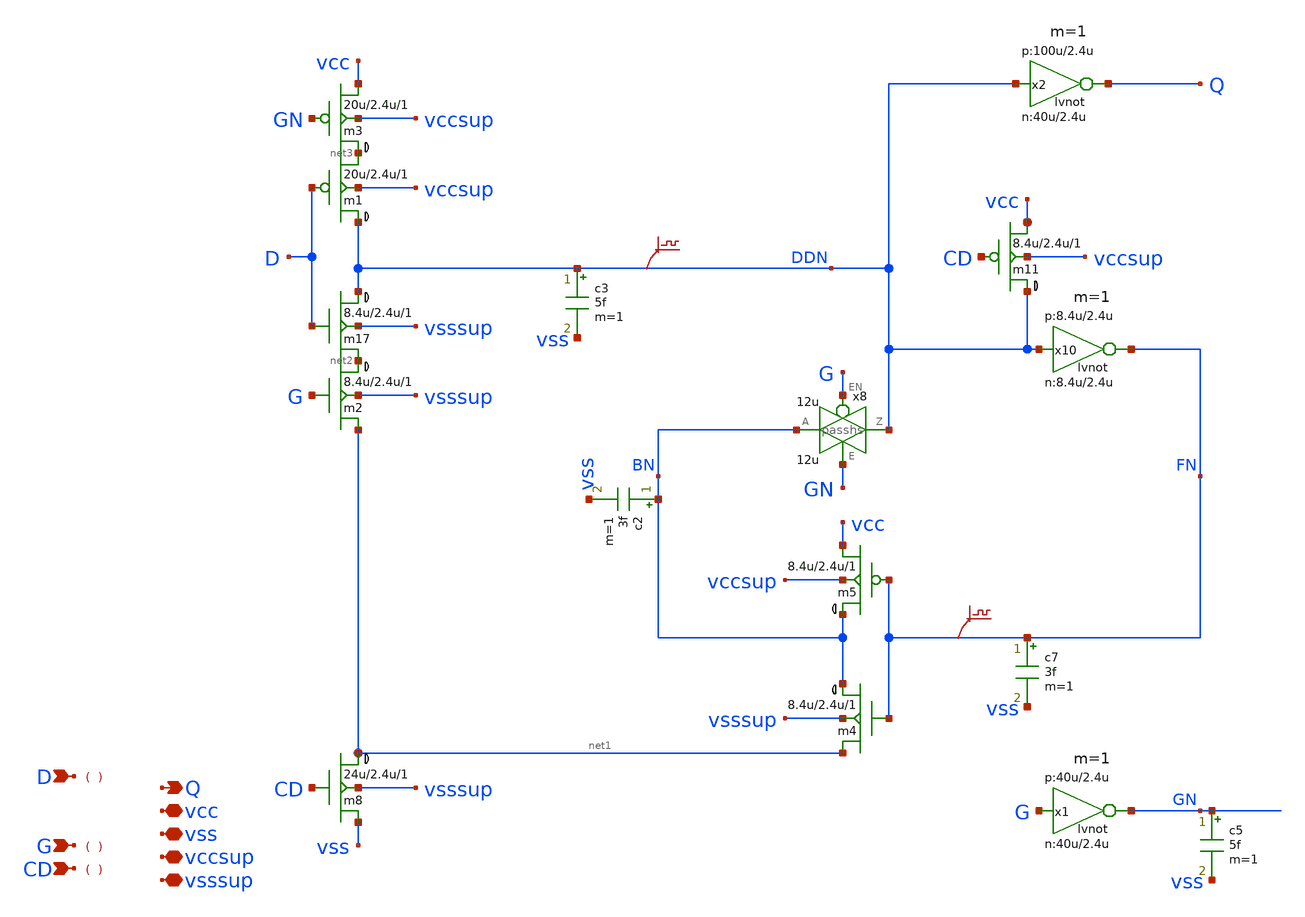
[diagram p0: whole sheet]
** sch_path: xschem-src/xschem_library/rom8k/LD2QHDX4stef.sch
* Copyright (C) 1998-2026 Stefan Frederik Schippers
* This program is free software; you can redistribute it and/or modify
* it under the terms of the GNU General Public License as published by
* the Free Software Foundation; either version 2 of the License, or
* (at your option) any later version.
* This program is distributed in the hope that it will be useful,
* but WITHOUT ANY WARRANTY; without even the implied warranty of
* MERCHANTABILITY or FITNESS FOR A PARTICULAR PURPOSE.  See the
* GNU General Public License for more details.
* You should have received a copy of the GNU General Public License
* along with this program; if not, write to the Free Software
**.subckt LD2QHDX4stef D G CD Q vcc vss vccsup vsssup
*.ipin D
*.ipin G
*.ipin CD
*.opin Q
*.iopin vcc
*.iopin vss
*.iopin vccsup
*.iopin vsssup
c2 BN vss 3f m=1
c3 DDN vss 5f m=1
c5 GN vss 5f m=1
c7 FN vss 3f m=1
x8 DDN BN G GN vccsup vsssup passhs WN=12u LN=1.2u WP=12u LP=1.2u
m17 DDN D net2 vsssup cmosn w=8.4u l=2.4u ad={8.4u *2.2u} as={8.4u *2.2u} pd={8.4u *2+4.4u} ps={8.4u *2+4.4u}
+ m=1
m1 DDN D net3 vccsup cmosp w=20u l=2.4u ad={20u *2.2u} as={20u *2.2u} pd={20u *2+4.4u} ps={20u *2+4.4u}
+ m=1
m2 net2 G net1 vsssup cmosn w=8.4u l=2.4u ad={8.4u *2.2u} as={8.4u *2.2u} pd={8.4u *2+4.4u} ps={8.4u *2+4.4u}
+ m=1
m3 net3 GN vcc vccsup cmosp w=20u l=2.4u ad={20u *2.2u} as={20u *2.2u} pd={20u *2+4.4u} ps={20u *2+4.4u}
+ m=1
m4 BN FN net1 vsssup cmosn w=8.4u l=2.4u ad={8.4u *2.2u} as={8.4u *2.2u} pd={8.4u *2+4.4u} ps={8.4u *2+4.4u}
+ m=1
m5 BN FN vcc vccsup cmosp w=8.4u l=2.4u ad={8.4u *2.2u} as={8.4u *2.2u} pd={8.4u *2+4.4u} ps={8.4u *2+4.4u}
+ m=1
m8 net1 CD vss vsssup cmosn w=24u l=2.4u ad={24u *2.2u} as={24u *2.2u} pd={24u *2+4.4u} ps={24u *2+4.4u}
+ m=1
m11 DDN CD vcc vccsup cmosp w=8.4u l=2.4u ad={8.4u *2.2u} as={8.4u *2.2u} pd={8.4u *2+4.4u} ps={8.4u *2+4.4u}
+ m=1
x10 FN DDN vcc vss lvnot wn=8.4u lln=2.4u wp=8.4u lp=2.4u m=1
x1 GN G vcc vss lvnot wn=40u lln=2.4u wp=40u lp=2.4u m=1
x2 Q DDN vcc vss lvnot wn=40u lln=2.4u wp=100u lp=2.4u m=1
.save v(ddn)
.save v(fn)
**.ends

* expanding   symbol:  passhs.sym # of pins=4
** sym_path: xschem-src/xschem_library/rom8k/passhs.sym
** sch_path: xschem-src/xschem_library/rom8k/passhs.sch
.subckt passhs Z A EN E VCCPIN VSSPIN  WN=2u LN=1.2u WP=2u LP=1.2u
*.iopin Z
*.iopin A
*.ipin EN
*.ipin E
m60 Z EN A VCCPIN cmosp w=WP l=2.4u ad='WP *4.6u' as='WP *4.6u' pd='WP *2+9.2u' ps='WP *2+9.2u' m=1
m1 A E Z VSSPIN cmosn w=WN l=2.4u ad='WN *4.3u' as='WN *4.3u' pd='WN *2+8.6u' ps='WN *2+8.6u' m=1
* noconn VSSPIN
* noconn VCCPIN
.ends


* expanding   symbol:  lvnot.sym # of pins=2
** sym_path: xschem-src/xschem_library/rom8k/lvnot.sym
** sch_path: xschem-src/xschem_library/rom8k/lvnot.sch
.subckt lvnot y a VCCPIN VSSPIN     wn=10u lln=1.2u wp=10u lp=1.2u
*.opin y
*.ipin a
m2 DP a VCCPIN VCCPIN cmosp w=wp l=lp ad='wp *4.6u' as='wp *4.6u' pd='wp *2+9.2u' ps='wp *2+9.2u' m=1
m1 DN a VSSPIN VSSPIN cmosn w=wn l=lln ad='wn *4.3u' as='wn *4.3u' pd='wn *2+8.6u' ps='wn *2+8.6u' m=1
Vmeas DP y 0
.save i(vmeas)
Vmeas1 y DN 0
.save i(vmeas1)
.save v(dp)
.save v(dn)
.ends

.end
